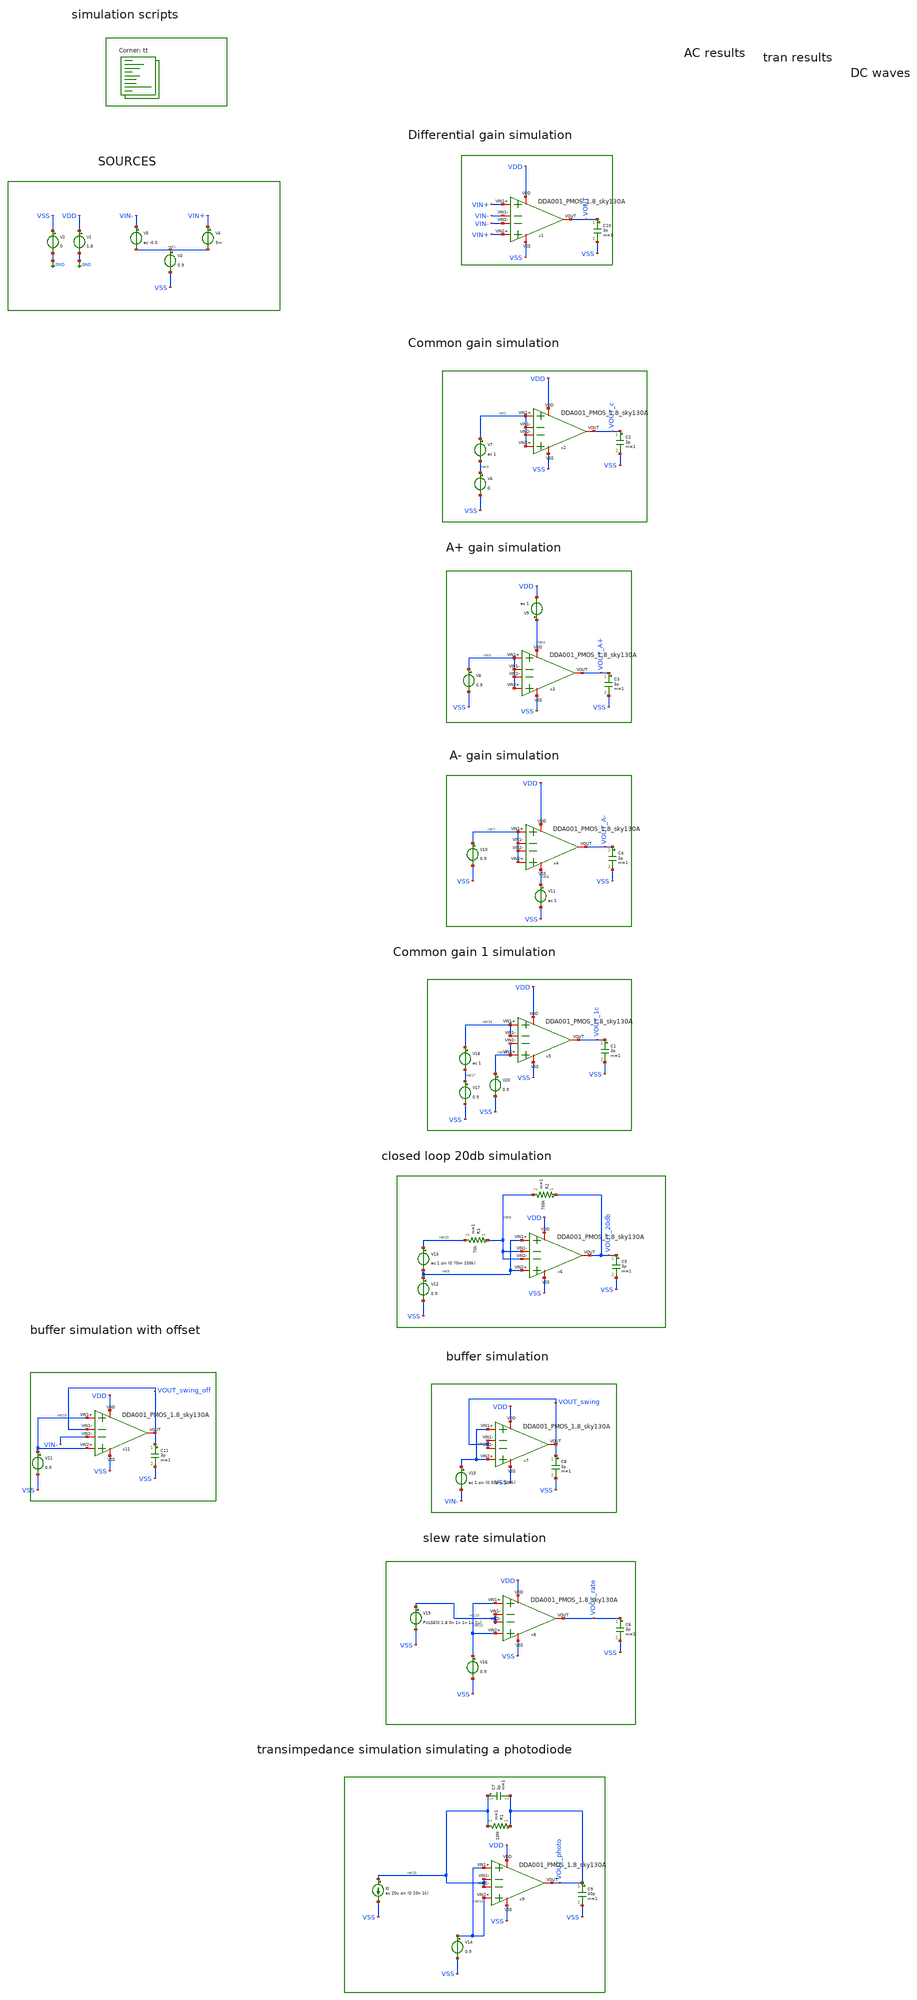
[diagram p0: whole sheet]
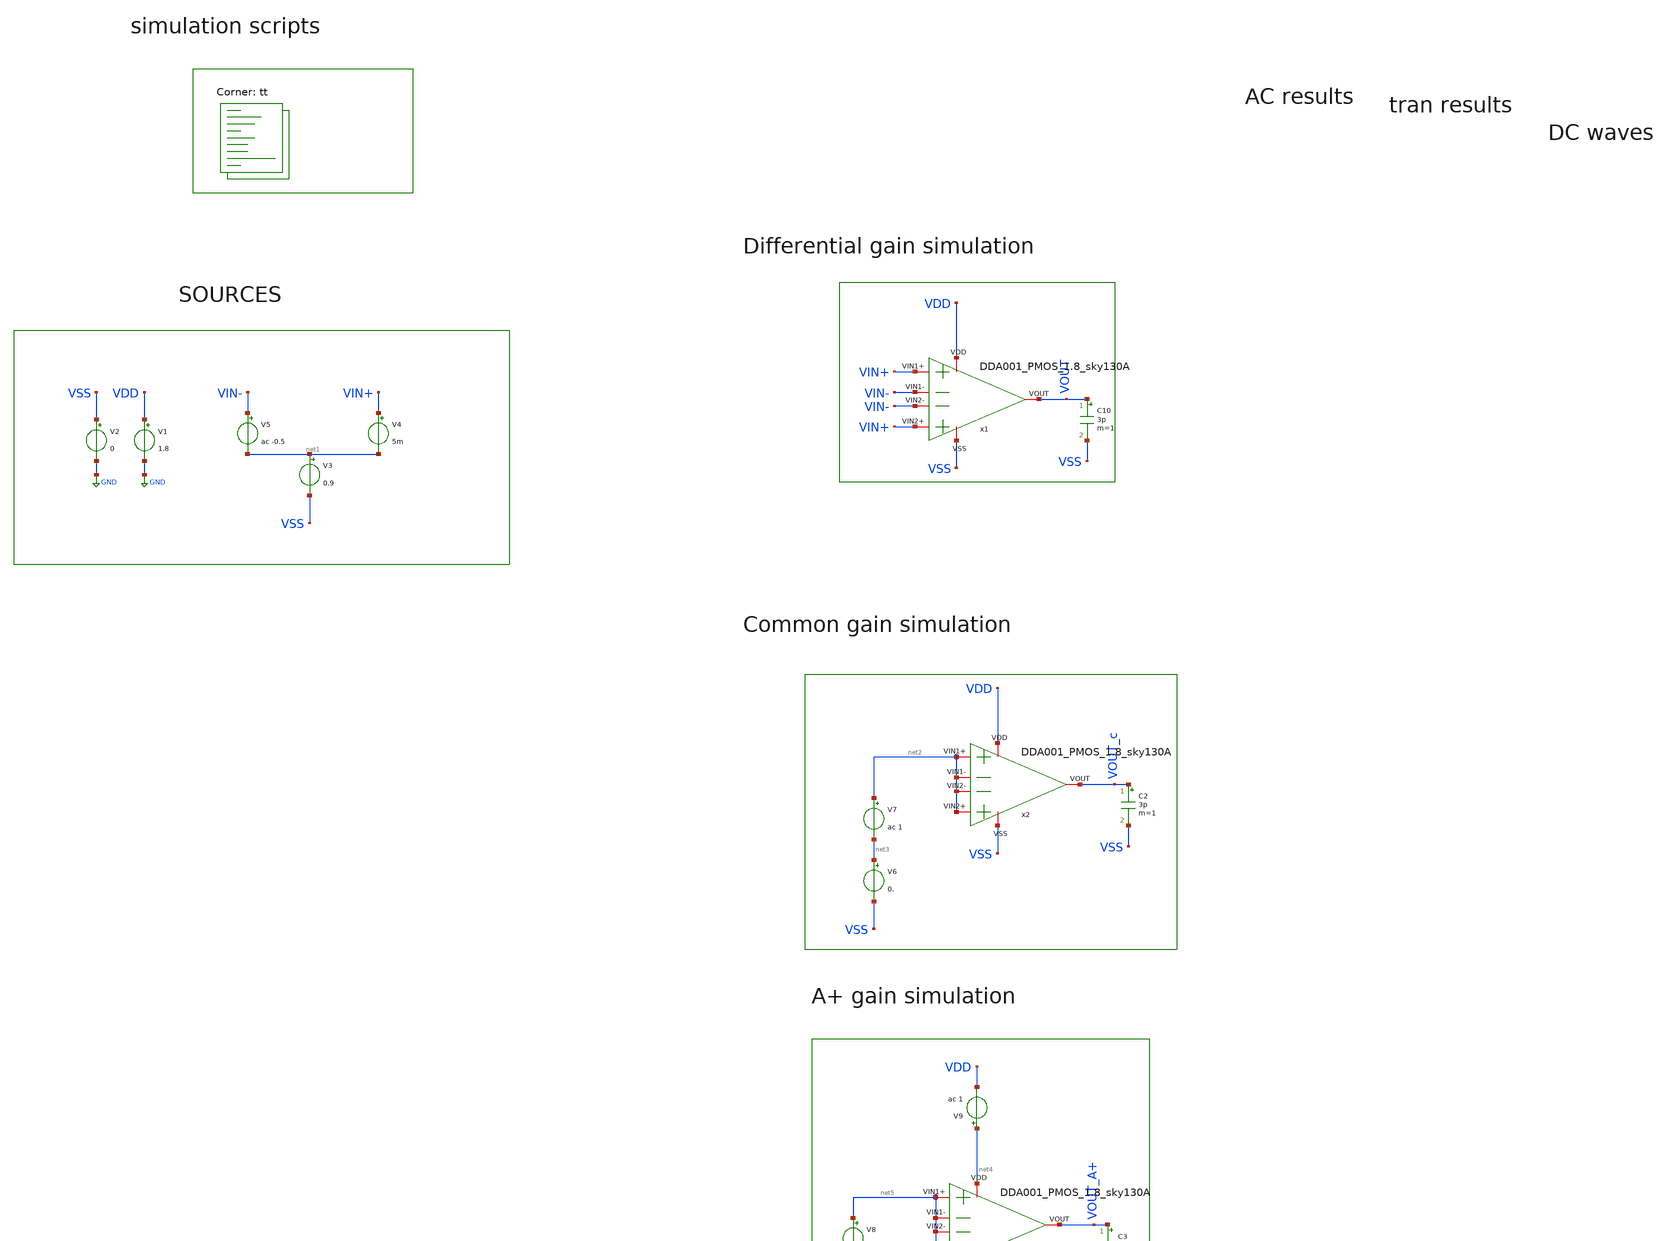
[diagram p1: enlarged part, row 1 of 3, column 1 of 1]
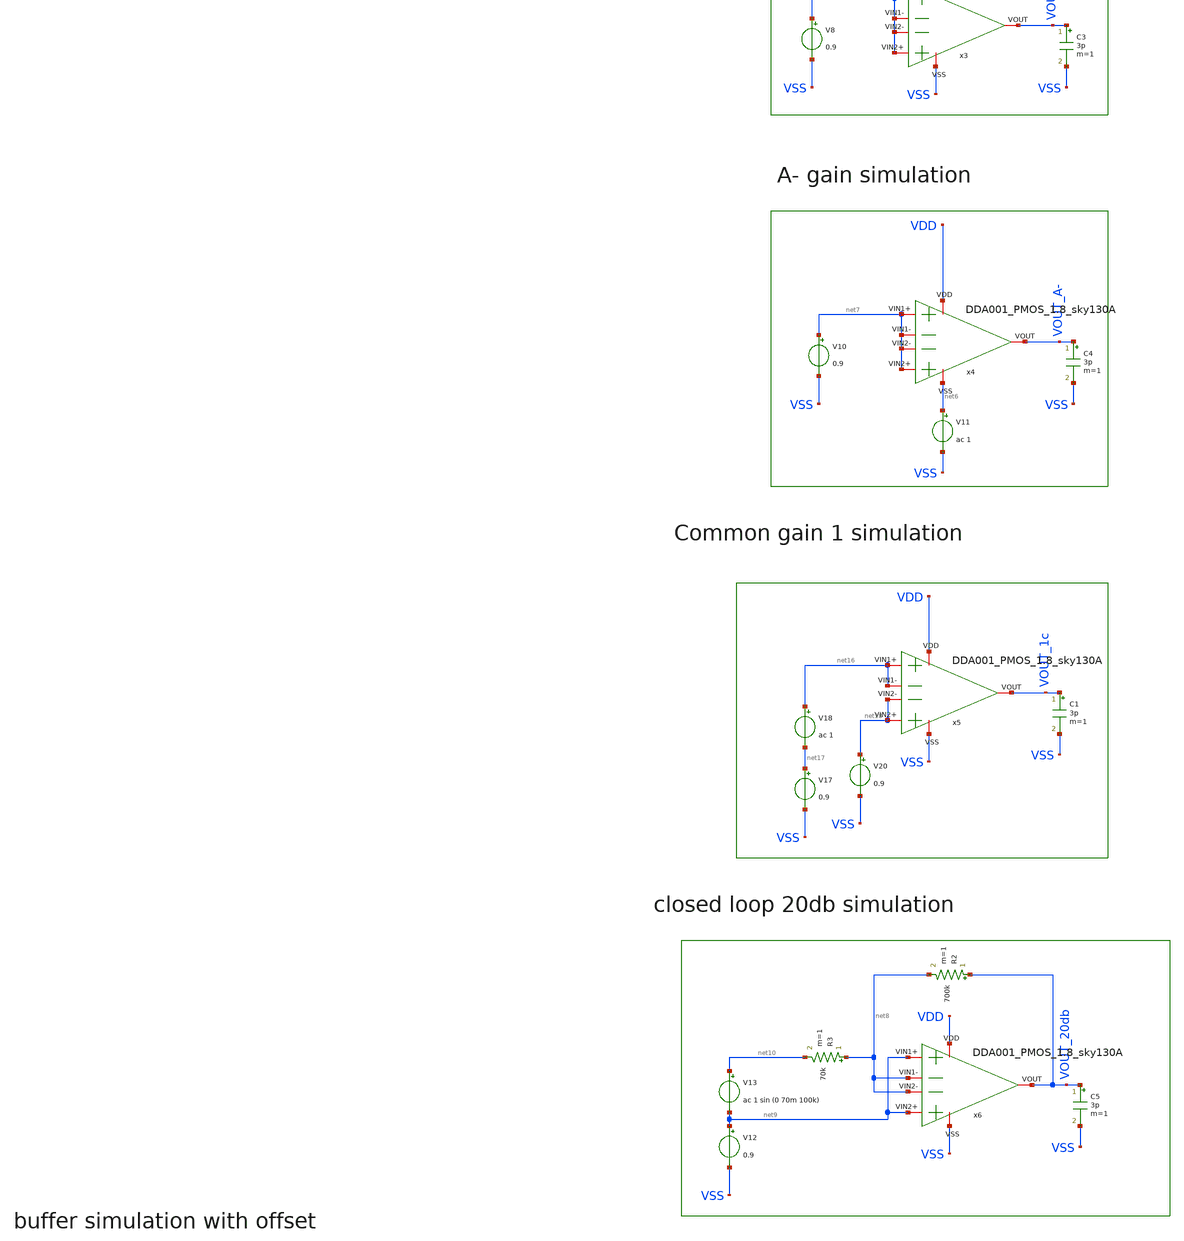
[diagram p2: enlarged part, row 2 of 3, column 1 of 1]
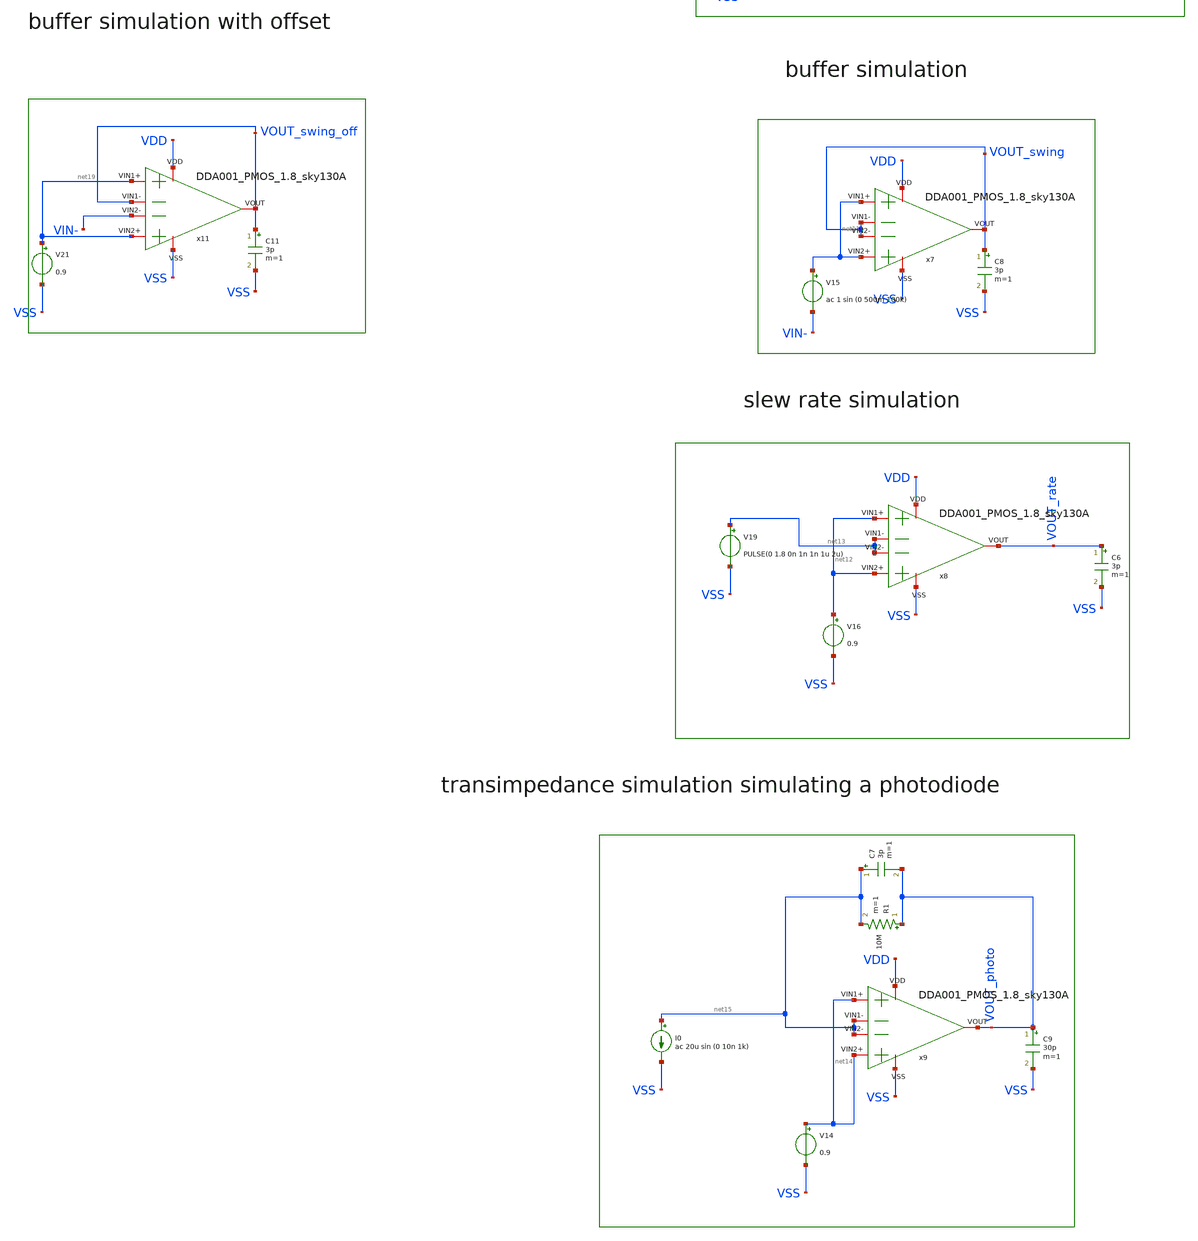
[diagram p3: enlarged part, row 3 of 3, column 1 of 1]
** sch_path: my_ip/testbenches_sky/DDA_testbenches/tb.sch
**.subckt tb
V1 VDD GND 1.8
V2 VSS GND 0
V3 net1 VSS 0.9
V4 VIN+ net1 5m
V5 VIN- net1 ac -0.5
C2 VOUT_c VSS 3p m=1
V6 net3 VSS 0.
V7 net2 net3 ac 1
C3 VOUT_A+ VSS 3p m=1
V8 net5 VSS 0.9
V9 net4 VDD ac 1
C4 VOUT_A- VSS 3p m=1
V10 net7 VSS 0.9
V11 net6 VSS ac 1
R2 VOUT_20db net8 700k m=1
R3 net8 net10 70k m=1
V12 net9 VSS 0.9
V13 net10 net9 ac 1 sin (0 70m 100k)
C5 VOUT_20db VSS 3p m=1
V15 net11 VIN- ac 1 sin (0 500m 100k)
V16 net12 VSS 0.9
C6 VOUT_rate VSS 3p m=1
V19 net13 VSS PULSE(0 1.8 0n 1n 1n 1u 2u)
C7 net15 VOUT_photo 3p m=1
V14 net14 VSS 0.9
R1 VOUT_photo net15 10M m=1
I0 net15 VSS ac 20u sin (0 10n 1k)
C8 VOUT_swing VSS 3p m=1
C9 VOUT_photo VSS 30p m=1
C10 VOUT VSS 3p m=1
C1 VOUT_1c VSS 3p m=1
V17 net17 VSS 0.9
V18 net16 net17 ac 1
V20 net18 VSS 0.9
C11 VOUT_swing_off VSS 3p m=1
V21 net19 VSS 0.9
x1 VDD VSS VIN- VIN+ VOUT VIN- VIN+ DDA001_PMOS_1.8_sky130A
x2 VDD VSS net2 net2 VOUT_c net2 net2 DDA001_PMOS_1.8_sky130A
x3 net4 VSS net5 net5 VOUT_A+ net5 net5 DDA001_PMOS_1.8_sky130A
x4 VDD net6 net7 net7 VOUT_A- net7 net7 DDA001_PMOS_1.8_sky130A
x5 VDD VSS net16 net16 VOUT_1c net18 net18 DDA001_PMOS_1.8_sky130A
x6 VDD VSS net8 net9 VOUT_20db net8 net9 DDA001_PMOS_1.8_sky130A
x7 VDD VSS VOUT_swing net11 VOUT_swing VOUT_swing net11 DDA001_PMOS_1.8_sky130A
x8 VDD VSS net13 net12 VOUT_rate net13 net12 DDA001_PMOS_1.8_sky130A
x9 VDD VSS net15 net14 VOUT_photo net15 net14 DDA001_PMOS_1.8_sky130A
x11 VDD VSS VOUT_swing_off net19 VOUT_swing_off VIN- net19 DDA001_PMOS_1.8_sky130A
**** begin user architecture code
.lib $::SKYWATER_MODELS/sky130.lib.spice tt

**************************************************************
**************************************************************
**************************************************************
**************************************************************
**************************************************************
*LIBs*********************************************************
**************************************************************
**************************************************************
**************************************************************
**************************************************************
**************************************************************
*.lib $::SKYWATER_MODELS/sky130.lib.spice tt
* chose the corners in the corner file
* tt_mm for mismatch
* ss ff sf fs standart corners
* ll hh lh hl capacitor and resistors corners
* mc for total process variation including corners
**************************************************************
**************************************************************
**************************************************************
**************************************************************
**************************************************************
*Corners/montecarlo options***********************************
**************************************************************
**************************************************************
**************************************************************
**************************************************************
**************************************************************
.TEMP 27
**************************************************************
**************************************************************
**************************************************************
**************************************************************
*SIMULATION and Plots*****************************************
**************************************************************
**************************************************************
**************************************************************
**************************************************************
.control
save all
save @m.x1.xm1.msky130_fd_pr__pfet_01v8_lvt[gm]
save @m.x1.xm1.msky130_fd_pr__pfet_01v8_lvt[vth]
save @m.x1.xm1.msky130_fd_pr__pfet_01v8_lvt[gds]
save @m.x1.xm1.msky130_fd_pr__pfet_01v8_lvt[gmbs]
save @m.x1.xm1.msky130_fd_pr__pfet_01v8_lvt[vds]
save @m.x1.xm1.msky130_fd_pr__pfet_01v8_lvt[vgs]


save @m.x1.xm2.msky130_fd_pr__pfet_01v8_lvt[gm]
save @m.x1.xm2.msky130_fd_pr__pfet_01v8_lvt[vth]
save @m.x1.xm2.msky130_fd_pr__pfet_01v8_lvt[gds]
save @m.x1.xm2.msky130_fd_pr__pfet_01v8_lvt[gmbs]
save @m.x1.xm2.msky130_fd_pr__pfet_01v8_lvt[vds]
save @m.x1.xm2.msky130_fd_pr__pfet_01v8_lvt[vgs]

save @m.x1.xm3.msky130_fd_pr__nfet_01v8[gm]
save @m.x1.xm3.msky130_fd_pr__nfet_01v8[vth]
save @m.x1.xm3.msky130_fd_pr__nfet_01v8[gds]
save @m.x1.xm3.msky130_fd_pr__nfet_01v8[gmbs]
save @m.x1.xm3.msky130_fd_pr__nfet_01v8[vds]
save @m.x1.xm3.msky130_fd_pr__nfet_01v8[vgs]

save @m.x1.xm4.msky130_fd_pr__nfet_01v8[gm]
save @m.x1.xm4.msky130_fd_pr__nfet_01v8[vth]
save @m.x1.xm4.msky130_fd_pr__nfet_01v8[gds]
save @m.x1.xm4.msky130_fd_pr__nfet_01v8[gmbs]
save @m.x1.xm4.msky130_fd_pr__nfet_01v8[vds]
save @m.x1.xm4.msky130_fd_pr__nfet_01v8[vgs]

save @m.x1.xm5.msky130_fd_pr__nfet_01v8[gm]
save @m.x1.xm5.msky130_fd_pr__nfet_01v8[vth]
save @m.x1.xm5.msky130_fd_pr__nfet_01v8[gds]
save @m.x1.xm5.msky130_fd_pr__nfet_01v8[gmbs]
save @m.x1.xm5.msky130_fd_pr__nfet_01v8[vds]
save @m.x1.xm5.msky130_fd_pr__nfet_01v8[vgs]

save @m.x1.xm6.msky130_fd_pr__nfet_01v8[gm]
save @m.x1.xm6.msky130_fd_pr__nfet_01v8[vth]
save @m.x1.xm6.msky130_fd_pr__nfet_01v8[gds]
save @m.x1.xm6.msky130_fd_pr__nfet_01v8[gmbs]
save @m.x1.xm6.msky130_fd_pr__nfet_01v8[vds]
save @m.x1.xm6.msky130_fd_pr__nfet_01v8[vgs]

save @m.x1.xm7.msky130_fd_pr__pfet_01v8_lvt[gm]
save @m.x1.xm7.msky130_fd_pr__pfet_01v8_lvt[vth]
save @m.x1.xm7.msky130_fd_pr__pfet_01v8_lvt[gds]
save @m.x1.xm7.msky130_fd_pr__pfet_01v8_lvt[gmbs]
save @m.x1.xm7.msky130_fd_pr__pfet_01v8_lvt[vds]
save @m.x1.xm7.msky130_fd_pr__pfet_01v8_lvt[vgs]

save @m.x1.xm8.msky130_fd_pr__pfet_01v8_lvt[gm]
save @m.x1.xm8.msky130_fd_pr__pfet_01v8_lvt[vth]
save @m.x1.xm8.msky130_fd_pr__pfet_01v8_lvt[gds]
save @m.x1.xm8.msky130_fd_pr__pfet_01v8_lvt[gmbs]
save @m.x1.xm8.msky130_fd_pr__pfet_01v8_lvt[vds]
save @m.x1.xm8.msky130_fd_pr__pfet_01v8_lvt[vgs]

save @m.x1.xm9.msky130_fd_pr__pfet_01v8_lvt[gm]
save @m.x1.xm9.msky130_fd_pr__pfet_01v8_lvt[vth]
save @m.x1.xm9.msky130_fd_pr__pfet_01v8_lvt[gds]
save @m.x1.xm9.msky130_fd_pr__pfet_01v8_lvt[gmbs]
save @m.x1.xm9.msky130_fd_pr__pfet_01v8_lvt[vds]
save @m.x1.xm9.msky130_fd_pr__pfet_01v8_lvt[vgs]


save @m.x1.xm10.msky130_fd_pr__nfet_01v8[gm]
save @m.x1.xm10.msky130_fd_pr__nfet_01v8[vth]
save @m.x1.xm10.msky130_fd_pr__nfet_01v8[gds]
save @m.x1.xm10.msky130_fd_pr__nfet_01v8[gmbs]
save @m.x1.xm10.msky130_fd_pr__nfet_01v8[vds]
save @m.x1.xm10.msky130_fd_pr__nfet_01v8[vgs]


save @m.x1.xm11.msky130_fd_pr__nfet_01v8[gm]
save @m.x1.xm11.msky130_fd_pr__nfet_01v8[vth]
save @m.x1.xm11.msky130_fd_pr__nfet_01v8[gds]
save @m.x1.xm11.msky130_fd_pr__nfet_01v8[gmbs]
save @m.x1.xm11.msky130_fd_pr__nfet_01v8[vds]
save @m.x1.xm11.msky130_fd_pr__nfet_01v8[vgs]

save @m.x1.xm12.msky130_fd_pr__pfet_01v8_lvt[gm]
save @m.x1.xm12.msky130_fd_pr__pfet_01v8_lvt[vth]
save @m.x1.xm12.msky130_fd_pr__pfet_01v8_lvt[gds]
save @m.x1.xm12.msky130_fd_pr__pfet_01v8_lvt[gmbs]
save @m.x1.xm12.msky130_fd_pr__pfet_01v8_lvt[vds]
save @m.x1.xm12.msky130_fd_pr__pfet_01v8_lvt[vgs]

save @m.x1.xm13.msky130_fd_pr__nfet_01v8[gm]
save @m.x1.xm13.msky130_fd_pr__nfet_01v8[vth]
save @m.x1.xm13.msky130_fd_pr__nfet_01v8[gds]
save @m.x1.xm13.msky130_fd_pr__nfet_01v8[gmbs]
save @m.x1.xm13.msky130_fd_pr__nfet_01v8[vds]
save @m.x1.xm13.msky130_fd_pr__nfet_01v8[vgs]

op
write tb.raw
set appendwrite

ac dec 10 1 50G
plot db(v(VOUT)) (180*ph(v(VOUT))/pi)
plot (db(v(VOUT))-db(v(VOUT_c)))
plot (db(v(VOUT))-db(v(VOUT_A+)))
plot (db(v(VOUT))-db(v(VOUT_A-)))
plot db(v(VOUT_amp))
set appendwrite
write tb.raw

tran 10ns 50u
set appendwrite
write tb.raw
noise v(VOUT,VSS) V4 dec 10 1 10G
set appendwrite
write tb.raw
plot inoise_spectrum

dc V3 0 1.8 0.001
plot v(VIN-)
set appendwrite
write tb.raw
.endc

**** end user architecture code
**.ends

* expanding   symbol:  DDA/DDA001_PMOS_1.8_sky130A .sym # of pins=7
** sym_path: LIB/Sky130A/DDA/DDA001_PMOS_1.8_sky130A .sym
** sch_path: LIB/Sky130A/DDA/DDA001_PMOS_1.8_sky130A .sch
.subckt DDA001_PMOS_1.8_sky130A  VDD VSS VIN1- VIN1+ VOUT VIN2- VIN2+
*.iopin VDD
*.iopin VSS
*.iopin VIN1-
*.iopin VIN1+
*.iopin VOUT
*.iopin VIN2-
*.iopin VIN2+
XM1 VB1 VB1 VDD VDD sky130_fd_pr__pfet_01v8_lvt L=1 W='3 * 4 ' nf=4 ad='int((4 + 1)/2) * 3 / 4 * 0.29'
+ as='int((4 + 2)/2) * 3 / 4 * 0.29' pd='2*int((4 + 1)/2) * (3 / 4 + 0.29)' ps='2*int((4 + 2)/2) * (3 / 4 + 0.29)'
+ nrd='0.29 / 3 ' nrs='0.29 / 3 ' sa=0 sb=0 sd=0 mult=2 m=2
XM2 VCFsdsd VB1 VDD VDD sky130_fd_pr__pfet_01v8_lvt L=1 W='3 * 4 ' nf=4 ad='int((4 + 1)/2) * 3 / 4 * 0.29'
+ as='int((4 + 2)/2) * 3 / 4 * 0.29' pd='2*int((4 + 1)/2) * (3 / 4 + 0.29)' ps='2*int((4 + 2)/2) * (3 / 4 + 0.29)'
+ nrd='0.29 / 3 ' nrs='0.29 / 3 ' sa=0 sb=0 sd=0 mult=16 m=16
XM3 net1 VB1 VDD VDD sky130_fd_pr__pfet_01v8_lvt L=1 W='3 * 4 ' nf=4 ad='int((4 + 1)/2) * 3 / 4 * 0.29'
+ as='int((4 + 2)/2) * 3 / 4 * 0.29' pd='2*int((4 + 1)/2) * (3 / 4 + 0.29)' ps='2*int((4 + 2)/2) * (3 / 4 + 0.29)'
+ nrd='0.29 / 3 ' nrs='0.29 / 3 ' sa=0 sb=0 sd=0 mult=16 m=16
XM4 VCF VIN1- VCFsdsd VDD sky130_fd_pr__pfet_01v8_lvt L=2 W='4 * 4 ' nf=4 ad='int((4 + 1)/2) * 4 / 4 * 0.29'
+ as='int((4 + 2)/2) * 4 / 4 * 0.29' pd='2*int((4 + 1)/2) * (4 / 4 + 0.29)' ps='2*int((4 + 2)/2) * (4 / 4 + 0.29)'
+ nrd='0.29 / 4 ' nrs='0.29 / 4 ' sa=0 sb=0 sd=0 mult=4 m=4
XM8 VCF VCF VSS VSS sky130_fd_pr__nfet_01v8 L=2 W='1 * 4 ' nf=4 ad='int((4 + 1)/2) * 1 / 4 * 0.29' as='int((4 + 2)/2) * 1 / 4 * 0.29'
+ pd='2*int((4 + 1)/2) * (1 / 4 + 0.29)' ps='2*int((4 + 2)/2) * (1 / 4 + 0.29)' nrd='0.29 / 1 ' nrs='0.29 / 1 '
+ sa=0 sb=0 sd=0 mult=2 m=2
XM9 VC VCF VSS VSS sky130_fd_pr__nfet_01v8 L=2 W='1 * 4 ' nf=4 ad='int((4 + 1)/2) * 1 / 4 * 0.29' as='int((4 + 2)/2) * 1 / 4 * 0.29'
+ pd='2*int((4 + 1)/2) * (1 / 4 + 0.29)' ps='2*int((4 + 2)/2) * (1 / 4 + 0.29)' nrd='0.29 / 1 ' nrs='0.29 / 1 '
+ sa=0 sb=0 sd=0 mult=2 m=2
XM10 VCFff VCFff VSS VSS sky130_fd_pr__nfet_01v8 L=2 W='1 * 4 ' nf=4 ad='int((4 + 1)/2) * 1 / 4 * 0.29'
+ as='int((4 + 2)/2) * 1 / 4 * 0.29' pd='2*int((4 + 1)/2) * (1 / 4 + 0.29)' ps='2*int((4 + 2)/2) * (1 / 4 + 0.29)'
+ nrd='0.29 / 1 ' nrs='0.29 / 1 ' sa=0 sb=0 sd=0 mult=2 m=2
XM11 VOUT VCFff VSS VSS sky130_fd_pr__nfet_01v8 L=2 W='1 * 4 ' nf=4 ad='int((4 + 1)/2) * 1 / 4 * 0.29'
+ as='int((4 + 2)/2) * 1 / 4 * 0.29' pd='2*int((4 + 1)/2) * (1 / 4 + 0.29)' ps='2*int((4 + 2)/2) * (1 / 4 + 0.29)'
+ nrd='0.29 / 1 ' nrs='0.29 / 1 ' sa=0 sb=0 sd=0 mult=2 m=2
XM12 VC VC VDD VDD sky130_fd_pr__pfet_01v8 L=1 W='4 * 4 ' nf=4 ad= as='int((4 + 2)/2) * 4 * 0.29' pd='2*int((4 + 1)/2) * (4 + 0.29)'
+ ps='2*int((4 + 2)/2) * (4 + 0.29)' nrd='0.29 / 4 / 4 ' nrs='0.29 / 4 / 4 ' sa=0 sb=0 sd=0 mult=2 m=2
XM13 VOUT VC VDD VDD sky130_fd_pr__pfet_01v8 L=1 W='4 * 4 ' nf=4 ad= as='int((4 + 2)/2) * 4 * 0.29' pd='2*int((4 + 1)/2) * (4 + 0.29)'
+ ps='2*int((4 + 2)/2) * (4 + 0.29)' nrd='0.29 / 4 / 4 ' nrs='0.29 / 4 / 4 ' sa=0 sb=0 sd=0 mult=2 m=2
XM5 VCF VIN2- net1 VDD sky130_fd_pr__pfet_01v8_lvt L=2 W='4 * 4 ' nf=4 ad='int((4 + 1)/2) * 4 / 4 * 0.29'
+ as='int((4 + 2)/2) * 4 / 4 * 0.29' pd='2*int((4 + 1)/2) * (4 / 4 + 0.29)' ps='2*int((4 + 2)/2) * (4 / 4 + 0.29)'
+ nrd='0.29 / 4 ' nrs='0.29 / 4 ' sa=0 sb=0 sd=0 mult=4 m=4
XM6 VCFff VIN1+ VCFsdsd VDD sky130_fd_pr__pfet_01v8_lvt L=2 W='4 * 4 ' nf=4 ad='int((4 + 1)/2) * 4 / 4 * 0.29'
+ as='int((4 + 2)/2) * 4 / 4 * 0.29' pd='2*int((4 + 1)/2) * (4 / 4 + 0.29)' ps='2*int((4 + 2)/2) * (4 / 4 + 0.29)'
+ nrd='0.29 / 4 ' nrs='0.29 / 4 ' sa=0 sb=0 sd=0 mult=4 m=4
XM7 VCFff VIN2+ net1 VDD sky130_fd_pr__pfet_01v8_lvt L=2 W='4 * 4 ' nf=4 ad='int((4 + 1)/2) * 4 / 4 * 0.29'
+ as='int((4 + 2)/2) * 4 / 4 * 0.29' pd='2*int((4 + 1)/2) * (4 / 4 + 0.29)' ps='2*int((4 + 2)/2) * (4 / 4 + 0.29)'
+ nrd='0.29 / 4 ' nrs='0.29 / 4 ' sa=0 sb=0 sd=0 mult=4 m=4
XR10 VSS net6 VSS sky130_fd_pr__res_xhigh_po_0p35 L=0.4 mult=2 m=2
XM14 net2 net3 net5 VSS sky130_fd_pr__nfet_01v8 L=3 W='2 * 2 ' nf=2 ad='int((2 + 1)/2) * 2 / 2 * 0.29'
+ as='int((2 + 2)/2) * 2 / 2 * 0.29' pd='2*int((2 + 1)/2) * (2 / 2 + 0.29)' ps='2*int((2 + 2)/2) * (2 / 2 + 0.29)'
+ nrd='0.29 / 2 ' nrs='0.29 / 2 ' sa=0 sb=0 sd=0 mult=4 m=4
XM15 net3 net3 net4 VSS sky130_fd_pr__nfet_01v8 L=3 W='2 * 2 ' nf=2 ad='int((2 + 1)/2) * 2 / 2 * 0.29'
+ as='int((2 + 2)/2) * 2 / 2 * 0.29' pd='2*int((2 + 1)/2) * (2 / 2 + 0.29)' ps='2*int((2 + 2)/2) * (2 / 2 + 0.29)'
+ nrd='0.29 / 2 ' nrs='0.29 / 2 ' sa=0 sb=0 sd=0 mult=4 m=4
XM16 net5 net4 net6 VSS sky130_fd_pr__nfet_01v8 L=2 W='3 * 2 ' nf=2 ad='int((2 + 1)/2) * 3 / 2 * 0.29'
+ as='int((2 + 2)/2) * 3 / 2 * 0.29' pd='2*int((2 + 1)/2) * (3 / 2 + 0.29)' ps='2*int((2 + 2)/2) * (3 / 2 + 0.29)'
+ nrd='0.29 / 3 ' nrs='0.29 / 3 ' sa=0 sb=0 sd=0 mult=8 m=8
XM17 net4 net4 VSS VSS sky130_fd_pr__nfet_01v8 L=2 W='3 * 2 ' nf=2 ad='int((2 + 1)/2) * 3 / 2 * 0.29'
+ as='int((2 + 2)/2) * 3 / 2 * 0.29' pd='2*int((2 + 1)/2) * (3 / 2 + 0.29)' ps='2*int((2 + 2)/2) * (3 / 2 + 0.29)'
+ nrd='0.29 / 3 ' nrs='0.29 / 3 ' sa=0 sb=0 sd=0 mult=2 m=2
XM18 net3 net2 VDD VDD sky130_fd_pr__pfet_01v8_lvt L=3 W='4 * 2 ' nf=2 ad='int((2 + 1)/2) * 4 / 2 * 0.29'
+ as='int((2 + 2)/2) * 4 / 2 * 0.29' pd='2*int((2 + 1)/2) * (4 / 2 + 0.29)' ps='2*int((2 + 2)/2) * (4 / 2 + 0.29)'
+ nrd='0.29 / 4 ' nrs='0.29 / 4 ' sa=0 sb=0 sd=0 mult=2 m=2
XM19 net2 net2 VDD VDD sky130_fd_pr__pfet_01v8_lvt L=3 W='4 * 2 ' nf=2 ad='int((2 + 1)/2) * 4 / 2 * 0.29'
+ as='int((2 + 2)/2) * 4 / 2 * 0.29' pd='2*int((2 + 1)/2) * (4 / 2 + 0.29)' ps='2*int((2 + 2)/2) * (4 / 2 + 0.29)'
+ nrd='0.29 / 4 ' nrs='0.29 / 4 ' sa=0 sb=0 sd=0 mult=2 m=2
XM20 VB1 net4 VSS VSS sky130_fd_pr__nfet_01v8 L=2 W='3 * 2 ' nf=2 ad='int((2 + 1)/2) * 3 / 2 * 0.29'
+ as='int((2 + 2)/2) * 3 / 2 * 0.29' pd='2*int((2 + 1)/2) * (3 / 2 + 0.29)' ps='2*int((2 + 2)/2) * (3 / 2 + 0.29)'
+ nrd='0.29 / 3 ' nrs='0.29 / 3 ' sa=0 sb=0 sd=0 mult=2 m=2
.ends

.GLOBAL GND
.end
